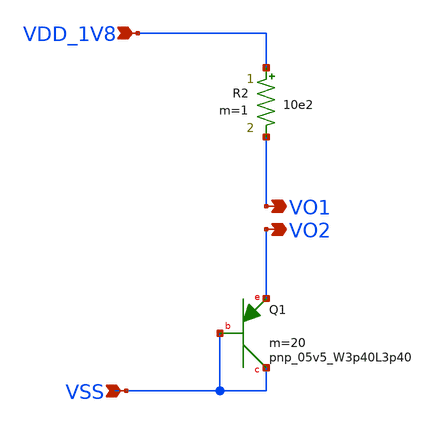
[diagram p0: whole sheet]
** sch_path: design/CNR_GR02_SKY130NM/CNR_GR02.sch
**.subckt CNR_GR02 VDD_1V8 VSS VO1 VO2
*.ipin VDD_1V8
*.ipin VSS
*.opin VO1
*.opin VO2
R2 VDD_1V8 VO1 10e2 m=1
XQ1 VSS VSS VO2 sky130_fd_pr__pnp_05v5_W3p40L3p40 m=20
**.ends
.end
